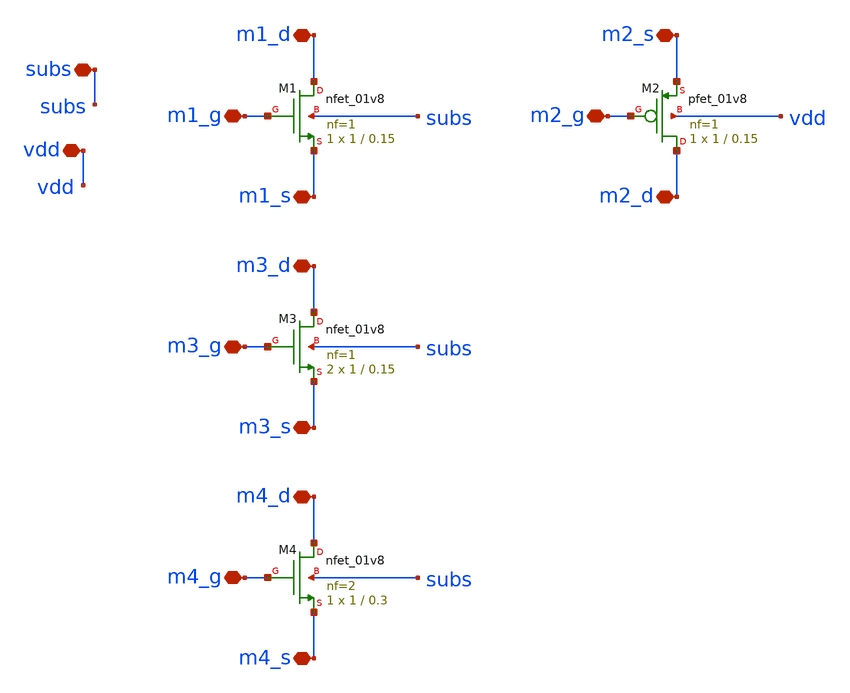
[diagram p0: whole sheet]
** sch_path: xschem/fets.sch
**.subckt fets subs vdd m1_d m1_s m1_g m2_s m2_d m2_g m3_d m3_s m3_g m4_d m4_s m4_g
*.iopin subs
*.iopin vdd
*.iopin m1_d
*.iopin m1_s
*.iopin m1_g
*.iopin m2_s
*.iopin m2_d
*.iopin m2_g
*.iopin m3_d
*.iopin m3_s
*.iopin m3_g
*.iopin m4_d
*.iopin m4_s
*.iopin m4_g
XM1 m1_d m1_g m1_s subs sky130_fd_pr__nfet_01v8 L=0.15 W=1 nf=1 ad='int((nf+1)/2) * W/nf * 0.29' as='int((nf+2)/2) * W/nf * 0.29'
+ pd='2*int((nf+1)/2) * (W/nf + 0.29)' ps='2*int((nf+2)/2) * (W/nf + 0.29)' nrd='0.29 / W' nrs='0.29 / W'
+ sa=0 sb=0 sd=0 mult=1 m=1
XM2 m2_d m2_g m2_s vdd sky130_fd_pr__pfet_01v8 L=0.15 W=1 nf=1 ad='int((nf+1)/2) * W/nf * 0.29' as='int((nf+2)/2) * W/nf * 0.29'
+ pd='2*int((nf+1)/2) * (W/nf + 0.29)' ps='2*int((nf+2)/2) * (W/nf + 0.29)' nrd='0.29 / W' nrs='0.29 / W'
+ sa=0 sb=0 sd=0 mult=1 m=1
XM3 m3_d m3_g m3_s subs sky130_fd_pr__nfet_01v8 L=0.15 W=1 nf=1 ad='int((nf+1)/2) * W/nf * 0.29' as='int((nf+2)/2) * W/nf * 0.29'
+ pd='2*int((nf+1)/2) * (W/nf + 0.29)' ps='2*int((nf+2)/2) * (W/nf + 0.29)' nrd='0.29 / W' nrs='0.29 / W'
+ sa=0 sb=0 sd=0 mult=2 m=2
XM4 m4_d m4_g m4_s subs sky130_fd_pr__nfet_01v8 L=0.3 W=1 nf=2 ad='int((nf+1)/2) * W/nf * 0.29' as='int((nf+2)/2) * W/nf * 0.29'
+ pd='2*int((nf+1)/2) * (W/nf + 0.29)' ps='2*int((nf+2)/2) * (W/nf + 0.29)' nrd='0.29 / W' nrs='0.29 / W'
+ sa=0 sb=0 sd=0 mult=1 m=1
**.ends
.end
